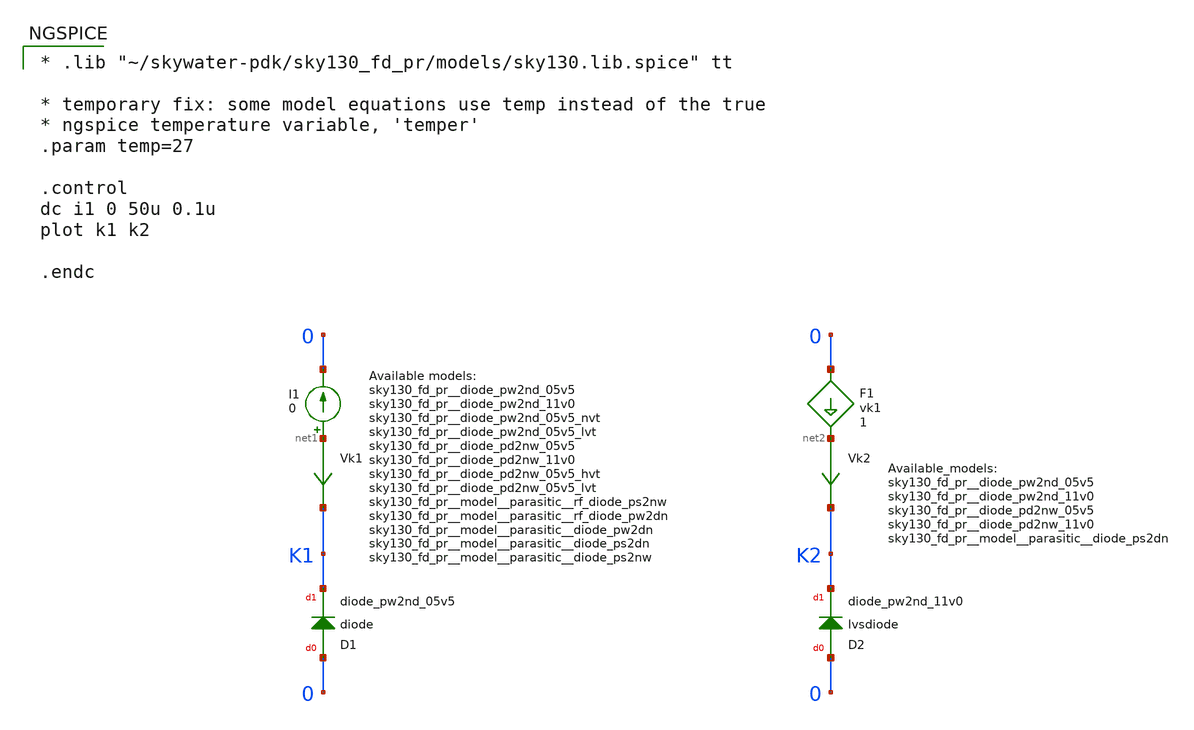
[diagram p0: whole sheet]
** sch_path: sky130_tests/test_diode.sch
* Copyright 2020 Stefan Frederik Schippers
* Licensed under the Apache License, Version 2.0 (the "License");
* you may not use this file except in compliance with the License.
* You may obtain a copy of the License at
* https://www.apache.org/licenses/LICENSE-2.0
* Unless required by applicable law or agreed to in writing, software
* distributed under the License is distributed on an "AS IS" BASIS,
* WITHOUT WARRANTIES OR CONDITIONS OF ANY KIND, either express or implied.
* See the License for the specific language governing permissions and
* limitations under the License.
**.subckt test_diode
I1 net1 0 0
Vk1 net1 K1 0
.save i(vk1)
D1 0 K1 sky130_fd_pr__diode_pw2nd_05v5 area=1
Vk2 net2 K2 0
.save i(vk2)
D2 0 K2 sky130_fd_pr__diode_pw2nd_11v0 area=1
F1 0 net2 vk1 1
**** begin user architecture code

* .lib "~/skywater-pdk/sky130_fd_pr/models/sky130.lib.spice" tt

* temporary fix: some model equations use temp instead of the true
* ngspice temperature variable, 'temper'
.param temp=27

.control
dc i1 0 50u 0.1u
plot k1 k2

.endc


**** end user architecture code
**.ends
**** begin user architecture code

.include   ~/skywater-pdk/sky130_fd_pr_ngspice/cells/nfet_01v8/sky130_fd_pr__nfet_01v8__tt.corner.spice
.include ~/skywater-pdk/sky130_fd_pr_ngspice/cells/nfet_01v8_lvt/sky130_fd_pr__nfet_01v8_lvt__tt.corner.spice
.include ~/skywater-pdk/sky130_fd_pr_ngspice/cells/pfet_01v8/sky130_fd_pr__pfet_01v8__tt.corner.spice
.include ~/skywater-pdk/sky130_fd_pr_ngspice/cells/nfet_03v3_nvt/sky130_fd_pr__nfet_03v3_nvt__tt.corner.spice
.include ~/skywater-pdk/sky130_fd_pr_ngspice/cells/nfet_05v0_nvt/sky130_fd_pr__nfet_05v0_nvt__tt.corner.spice
.include ~/skywater-pdk/sky130_fd_pr_ngspice/cells/esd_nfet_01v8/sky130_fd_pr__esd_nfet_01v8__tt.corner.spice
.include ~/skywater-pdk/sky130_fd_pr_ngspice/cells/pfet_01v8_lvt/sky130_fd_pr__pfet_01v8_lvt__tt.corner.spice
.include ~/skywater-pdk/sky130_fd_pr_ngspice/cells/pfet_01v8_hvt/sky130_fd_pr__pfet_01v8_hvt__tt.corner.spice
.include ~/skywater-pdk/sky130_fd_pr_ngspice/cells/esd_pfet_g5v0d10v5/sky130_fd_pr__esd_pfet_g5v0d10v5__tt.corner.spice
.include ~/skywater-pdk/sky130_fd_pr_ngspice/cells/pfet_g5v0d10v5/sky130_fd_pr__pfet_g5v0d10v5__tt.corner.spice
.include ~/skywater-pdk/sky130_fd_pr_ngspice/cells/pfet_g5v0d16v0/sky130_fd_pr__pfet_g5v0d16v0__tt.corner.spice
.include ~/skywater-pdk/sky130_fd_pr_ngspice/cells/nfet_g5v0d10v5/sky130_fd_pr__nfet_g5v0d10v5__tt.corner.spice
.include ~/skywater-pdk/sky130_fd_pr_ngspice/cells/nfet_g5v0d16v0/sky130_fd_pr__nfet_g5v0d16v0__tt_discrete.corner.spice
.include ~/skywater-pdk/sky130_fd_pr_ngspice/cells/esd_nfet_g5v0d10v5/sky130_fd_pr__esd_nfet_g5v0d10v5__tt.corner.spice
.include ~/skywater-pdk/sky130_fd_pr_ngspice/models/corners/tt/nonfet.spice
* Mismatch parameters
.include ~/skywater-pdk/sky130_fd_pr_ngspice/cells/nfet_01v8/sky130_fd_pr__nfet_01v8__mismatch.corner.spice
.include ~/skywater-pdk/sky130_fd_pr_ngspice/cells/pfet_01v8/sky130_fd_pr__pfet_01v8__mismatch.corner.spice
.include ~/skywater-pdk/sky130_fd_pr_ngspice/cells/nfet_01v8_lvt/sky130_fd_pr__nfet_01v8_lvt__mismatch.corner.spice
.include ~/skywater-pdk/sky130_fd_pr_ngspice/cells/pfet_01v8_lvt/sky130_fd_pr__pfet_01v8_lvt__mismatch.corner.spice
.include ~/skywater-pdk/sky130_fd_pr_ngspice/cells/pfet_01v8_hvt/sky130_fd_pr__pfet_01v8_hvt__mismatch.corner.spice
.include ~/skywater-pdk/sky130_fd_pr_ngspice/cells/nfet_g5v0d10v5/sky130_fd_pr__nfet_g5v0d10v5__mismatch.corner.spice
.include ~/skywater-pdk/sky130_fd_pr_ngspice/cells/pfet_g5v0d10v5/sky130_fd_pr__pfet_g5v0d10v5__mismatch.corner.spice
.include ~/skywater-pdk/sky130_fd_pr_ngspice/cells/nfet_05v0_nvt/sky130_fd_pr__nfet_05v0_nvt__mismatch.corner.spice
.include ~/skywater-pdk/sky130_fd_pr_ngspice/cells/nfet_03v3_nvt/sky130_fd_pr__nfet_03v3_nvt__mismatch.corner.spice
* Resistor/Capacitor
.include ~/skywater-pdk/sky130_fd_pr_ngspice/models/r+c/res_typical__cap_typical.spice
.include ~/skywater-pdk/sky130_fd_pr_ngspice/models/r+c/res_typical__cap_typical__lin.spice
* Special cells
.include ~/skywater-pdk/sky130_fd_pr_ngspice/models/corners/tt/specialized_cells.spice
* All models
.include ~/skywater-pdk/sky130_fd_pr_ngspice/models/all.spice
* Corner
.include ~/skywater-pdk/sky130_fd_pr_ngspice/models/corners/tt/rf.spice


**** end user architecture code
.end
